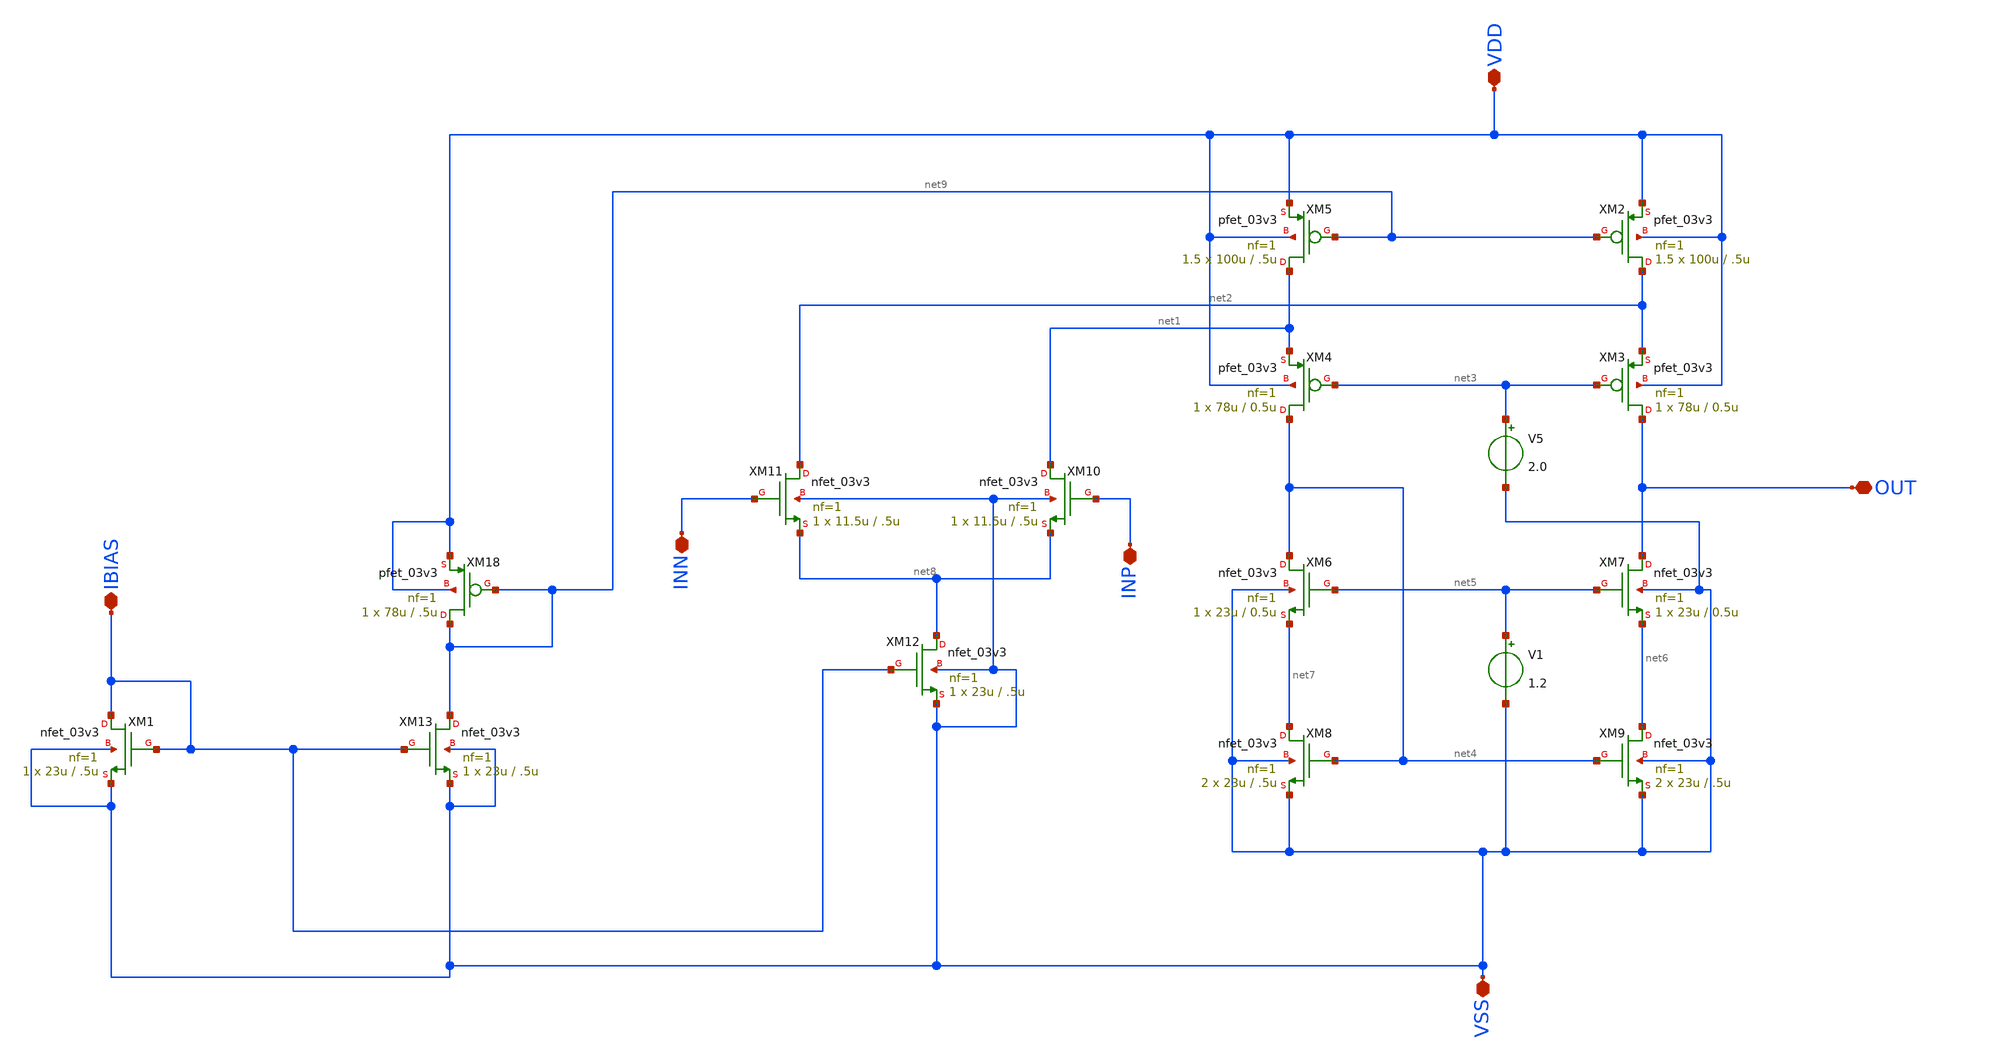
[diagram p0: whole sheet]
** sch_path: designs/libs/core_amps/ota_folded_cascode/symbol_from.sch
**.subckt symbol_from IBIAS INN INP OUT VSS VDD
*.iopin IBIAS
*.iopin INN
*.iopin INP
*.iopin OUT
*.iopin VSS
*.iopin VDD
XM1 IBIAS IBIAS VSS VSS nfet_03v3 L=.5u W=23u nf=1 ad='int((nf+1)/2) * W/nf * 0.18u' as='int((nf+2)/2) * W/nf * 0.18u'
+ pd='2*int((nf+1)/2) * (W/nf + 0.18u)' ps='2*int((nf+2)/2) * (W/nf + 0.18u)' nrd='0.18u / W' nrs='0.18u / W'
+ sa=0 sb=0 sd=0 m=1
XM2 net2 net9 VDD VDD pfet_03v3 L=.5u W=100u nf=1 ad='int((nf+1)/2) * W/nf * 0.18u' as='int((nf+2)/2) * W/nf * 0.18u'
+ pd='2*int((nf+1)/2) * (W/nf + 0.18u)' ps='2*int((nf+2)/2) * (W/nf + 0.18u)' nrd='0.18u / W' nrs='0.18u / W'
+ sa=0 sb=0 sd=0 m=1.5
XM3 OUT net3 net2 VDD pfet_03v3 L=0.5u W=78u nf=1 ad='int((nf+1)/2) * W/nf * 0.18u' as='int((nf+2)/2) * W/nf * 0.18u'
+ pd='2*int((nf+1)/2) * (W/nf + 0.18u)' ps='2*int((nf+2)/2) * (W/nf + 0.18u)' nrd='0.18u / W' nrs='0.18u / W'
+ sa=0 sb=0 sd=0 m=1
XM4 net4 net3 net1 VDD pfet_03v3 L=0.5u W=78u nf=1 ad='int((nf+1)/2) * W/nf * 0.18u' as='int((nf+2)/2) * W/nf * 0.18u'
+ pd='2*int((nf+1)/2) * (W/nf + 0.18u)' ps='2*int((nf+2)/2) * (W/nf + 0.18u)' nrd='0.18u / W' nrs='0.18u / W'
+ sa=0 sb=0 sd=0 m=1
XM5 net1 net9 VDD VDD pfet_03v3 L=.5u W=100u nf=1 ad='int((nf+1)/2) * W/nf * 0.18u' as='int((nf+2)/2) * W/nf * 0.18u'
+ pd='2*int((nf+1)/2) * (W/nf + 0.18u)' ps='2*int((nf+2)/2) * (W/nf + 0.18u)' nrd='0.18u / W' nrs='0.18u / W'
+ sa=0 sb=0 sd=0 m=1.5
XM6 net4 net5 net7 VSS nfet_03v3 L=0.5u W=23u nf=1 ad='int((nf+1)/2) * W/nf * 0.18u' as='int((nf+2)/2) * W/nf * 0.18u'
+ pd='2*int((nf+1)/2) * (W/nf + 0.18u)' ps='2*int((nf+2)/2) * (W/nf + 0.18u)' nrd='0.18u / W' nrs='0.18u / W'
+ sa=0 sb=0 sd=0 m=1
XM7 OUT net5 net6 VSS nfet_03v3 L=0.5u W=23u nf=1 ad='int((nf+1)/2) * W/nf * 0.18u' as='int((nf+2)/2) * W/nf * 0.18u'
+ pd='2*int((nf+1)/2) * (W/nf + 0.18u)' ps='2*int((nf+2)/2) * (W/nf + 0.18u)' nrd='0.18u / W' nrs='0.18u / W'
+ sa=0 sb=0 sd=0 m=1
XM8 net7 net4 VSS VSS nfet_03v3 L=.5u W=23u nf=1 ad='int((nf+1)/2) * W/nf * 0.18u' as='int((nf+2)/2) * W/nf * 0.18u'
+ pd='2*int((nf+1)/2) * (W/nf + 0.18u)' ps='2*int((nf+2)/2) * (W/nf + 0.18u)' nrd='0.18u / W' nrs='0.18u / W'
+ sa=0 sb=0 sd=0 m=2
XM9 net6 net4 VSS VSS nfet_03v3 L=.5u W=23u nf=1 ad='int((nf+1)/2) * W/nf * 0.18u' as='int((nf+2)/2) * W/nf * 0.18u'
+ pd='2*int((nf+1)/2) * (W/nf + 0.18u)' ps='2*int((nf+2)/2) * (W/nf + 0.18u)' nrd='0.18u / W' nrs='0.18u / W'
+ sa=0 sb=0 sd=0 m=2
XM10 net1 INP net8 VSS nfet_03v3 L=.5u W=11.5u nf=1 ad='int((nf+1)/2) * W/nf * 0.18u' as='int((nf+2)/2) * W/nf * 0.18u'
+ pd='2*int((nf+1)/2) * (W/nf + 0.18u)' ps='2*int((nf+2)/2) * (W/nf + 0.18u)' nrd='0.18u / W' nrs='0.18u / W'
+ sa=0 sb=0 sd=0 m=1
XM12 net8 IBIAS VSS VSS nfet_03v3 L=.5u W=23u nf=1 ad='int((nf+1)/2) * W/nf * 0.18u' as='int((nf+2)/2) * W/nf * 0.18u'
+ pd='2*int((nf+1)/2) * (W/nf + 0.18u)' ps='2*int((nf+2)/2) * (W/nf + 0.18u)' nrd='0.18u / W' nrs='0.18u / W'
+ sa=0 sb=0 sd=0 m=1
XM18 net9 net9 VDD VDD pfet_03v3 L=.5u W=78u nf=1 ad='int((nf+1)/2) * W/nf * 0.18u' as='int((nf+2)/2) * W/nf * 0.18u'
+ pd='2*int((nf+1)/2) * (W/nf + 0.18u)' ps='2*int((nf+2)/2) * (W/nf + 0.18u)' nrd='0.18u / W' nrs='0.18u / W'
+ sa=0 sb=0 sd=0 m=1
XM11 net2 INN net8 VSS nfet_03v3 L=.5u W=11.5u nf=1 ad='int((nf+1)/2) * W/nf * 0.18u' as='int((nf+2)/2) * W/nf * 0.18u'
+ pd='2*int((nf+1)/2) * (W/nf + 0.18u)' ps='2*int((nf+2)/2) * (W/nf + 0.18u)' nrd='0.18u / W' nrs='0.18u / W'
+ sa=0 sb=0 sd=0 m=1
XM13 net9 IBIAS VSS VSS nfet_03v3 L=.5u W=23u nf=1 ad='int((nf+1)/2) * W/nf * 0.18u' as='int((nf+2)/2) * W/nf * 0.18u'
+ pd='2*int((nf+1)/2) * (W/nf + 0.18u)' ps='2*int((nf+2)/2) * (W/nf + 0.18u)' nrd='0.18u / W' nrs='0.18u / W'
+ sa=0 sb=0 sd=0 m=1
V5 net3 VSS 2.0
V1 net5 VSS 1.2
**.ends
.end
